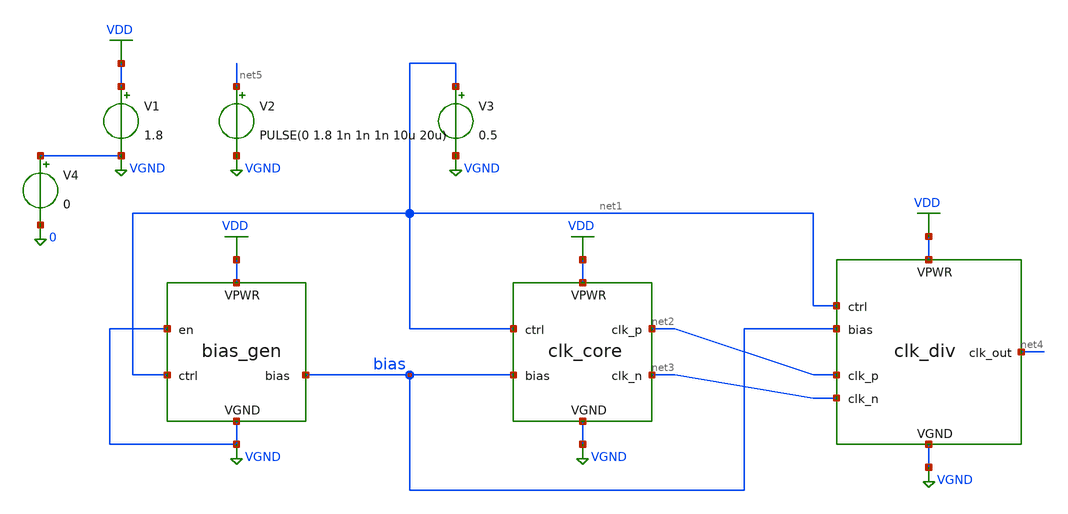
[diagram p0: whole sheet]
** sch_path: simple_vco/v1/tb_proto.sch
**.subckt tb_proto
x1 VDD VGND VGND net1 bias bias_gen
x2 VDD VGND net1 bias net2 net3 clk_core
x3 VDD VGND net1 bias net2 net3 net4 clk_div
V1 VDD VGND 1.8
V2 net5 VGND PULSE(0 1.8 1n 1n 1n 10u 20u)
V3 net1 VGND 0.5
V4 VGND 0 0
**** begin user architecture code


** opencircuitdesign pdks install

.lib $::SKYWATER_MODELS/sky130.lib.spice tt

.include $::SKYWATER_STDCELLS/sky130_fd_sc_hd.spice





.param mc_mm_switch=0

.control

save all

tran 50p 5u

plot CLK_OUT CLK_P CLK_N
plot bias

*quit 0

.endc

.end



**** end user architecture code
**.ends

* expanding   symbol:  bias_gen.sym # of pins=5
** sym_path: simple_vco/v1/bias_gen.sym
** sch_path: simple_vco/v1/bias_gen.sch
.subckt bias_gen VPWR VGND en ctrl bias_out
*.iopin VPWR
*.iopin VGND
*.ipin en
*.ipin ctrl
*.opin bias_out
XM8 net5 net5 VPWR VPWR sky130_fd_pr__pfet_01v8 L=0.15 W=1 nf=1 ad='int((1 + 1)/2) * 1 / 1 * 0.29' as='int((1 + 2)/2) * 1 / 1 * 0.29'
+ pd='2*int((1 + 1)/2) * (1 / 1 + 0.29)' ps='2*int((1 + 2)/2) * (1 / 1 + 0.29)' nrd='0.29 / 1 ' nrs='0.29 / 1 '
+ sa=0 sb=0 sd=0 mult=1 m=1
XM7 bias_out ctrl net3 VPWR sky130_fd_pr__pfet_01v8 L=0.15 W=1 nf=1 ad='int((1 + 1)/2) * 1 / 1 * 0.29'
+ as='int((1 + 2)/2) * 1 / 1 * 0.29' pd='2*int((1 + 1)/2) * (1 / 1 + 0.29)' ps='2*int((1 + 2)/2) * (1 / 1 + 0.29)'
+ nrd='0.29 / 1 ' nrs='0.29 / 1 ' sa=0 sb=0 sd=0 mult=1 m=1
XM6 net4 net1 net3 VPWR sky130_fd_pr__pfet_01v8 L=0.15 W=1 nf=1 ad='int((1 + 1)/2) * 1 / 1 * 0.29' as='int((1 + 2)/2) * 1 / 1 * 0.29'
+ pd='2*int((1 + 1)/2) * (1 / 1 + 0.29)' ps='2*int((1 + 2)/2) * (1 / 1 + 0.29)' nrd='0.29 / 1 ' nrs='0.29 / 1 '
+ sa=0 sb=0 sd=0 mult=1 m=1
XM3 net1 ctrl VPWR VPWR sky130_fd_pr__pfet_01v8 L=0.15 W=1 nf=1 ad='int((1 + 1)/2) * 1 / 1 * 0.29' as='int((1 + 2)/2) * 1 / 1 * 0.29'
+ pd='2*int((1 + 1)/2) * (1 / 1 + 0.29)' ps='2*int((1 + 2)/2) * (1 / 1 + 0.29)' nrd='0.29 / 1 ' nrs='0.29 / 1 '
+ sa=0 sb=0 sd=0 mult=1 m=1
XM1 net1 net1 VPWR VPWR sky130_fd_pr__pfet_01v8 L=0.15 W=1 nf=1 ad='int((1 + 1)/2) * 1 / 1 * 0.29' as='int((1 + 2)/2) * 1 / 1 * 0.29'
+ pd='2*int((1 + 1)/2) * (1 / 1 + 0.29)' ps='2*int((1 + 2)/2) * (1 / 1 + 0.29)' nrd='0.29 / 1 ' nrs='0.29 / 1 '
+ sa=0 sb=0 sd=0 mult=1 m=1
XM5 net3 net5 VPWR VPWR sky130_fd_pr__pfet_01v8 L=0.15 W=1 nf=1 ad='int((1 + 1)/2) * 1 / 1 * 0.29' as='int((1 + 2)/2) * 1 / 1 * 0.29'
+ pd='2*int((1 + 1)/2) * (1 / 1 + 0.29)' ps='2*int((1 + 2)/2) * (1 / 1 + 0.29)' nrd='0.29 / 1 ' nrs='0.29 / 1 '
+ sa=0 sb=0 sd=0 mult=1 m=1
XM9 bias_out net4 VGND VGND sky130_fd_pr__nfet_01v8 L=0.15 W=1 nf=1 ad='int((1 + 1)/2) * 1 / 1 * 0.29'
+ as='int((1 + 2)/2) * 1 / 1 * 0.29' pd='2*int((1 + 1)/2) * (1 / 1 + 0.29)' ps='2*int((1 + 2)/2) * (1 / 1 + 0.29)'
+ nrd='0.29 / 1 ' nrs='0.29 / 1 ' sa=0 sb=0 sd=0 mult=1 m=1
XM10 net4 net4 VGND VGND sky130_fd_pr__nfet_01v8 L=0.15 W=1 nf=1 ad='int((1 + 1)/2) * 1 / 1 * 0.29' as='int((1 + 2)/2) * 1 / 1 * 0.29'
+ pd='2*int((1 + 1)/2) * (1 / 1 + 0.29)' ps='2*int((1 + 2)/2) * (1 / 1 + 0.29)' nrd='0.29 / 1 ' nrs='0.29 / 1 '
+ sa=0 sb=0 sd=0 mult=1 m=1
XM11 net5 VPWR net6 VGND sky130_fd_pr__nfet_01v8 L=0.15 W=1 nf=1 ad='int((1 + 1)/2) * 1 / 1 * 0.29' as='int((1 + 2)/2) * 1 / 1 * 0.29'
+ pd='2*int((1 + 1)/2) * (1 / 1 + 0.29)' ps='2*int((1 + 2)/2) * (1 / 1 + 0.29)' nrd='0.29 / 1 ' nrs='0.29 / 1 '
+ sa=0 sb=0 sd=0 mult=1 m=1
XM12 net6 bias_out VGND VGND sky130_fd_pr__nfet_01v8 L=0.15 W=1 nf=1 ad='int((1 + 1)/2) * 1 / 1 * 0.29'
+ as='int((1 + 2)/2) * 1 / 1 * 0.29' pd='2*int((1 + 1)/2) * (1 / 1 + 0.29)' ps='2*int((1 + 2)/2) * (1 / 1 + 0.29)'
+ nrd='0.29 / 1 ' nrs='0.29 / 1 ' sa=0 sb=0 sd=0 mult=1 m=1
XM13 net6 net7 VGND VGND sky130_fd_pr__nfet_01v8 L=0.15 W=1 nf=1 ad='int((1 + 1)/2) * 1 / 1 * 0.29' as='int((1 + 2)/2) * 1 / 1 * 0.29'
+ pd='2*int((1 + 1)/2) * (1 / 1 + 0.29)' ps='2*int((1 + 2)/2) * (1 / 1 + 0.29)' nrd='0.29 / 1 ' nrs='0.29 / 1 '
+ sa=0 sb=0 sd=0 mult=1 m=1
XM14 net7 net8 VPWR VPWR sky130_fd_pr__pfet_01v8 L=0.15 W=1 nf=1 ad='int((1 + 1)/2) * 1 / 1 * 0.29' as='int((1 + 2)/2) * 1 / 1 * 0.29'
+ pd='2*int((1 + 1)/2) * (1 / 1 + 0.29)' ps='2*int((1 + 2)/2) * (1 / 1 + 0.29)' nrd='0.29 / 1 ' nrs='0.29 / 1 '
+ sa=0 sb=0 sd=0 mult=1 m=1
XM15 net7 net8 VGND VGND sky130_fd_pr__nfet_01v8 L=0.15 W=1 nf=1 ad='int((1 + 1)/2) * 1 / 1 * 0.29' as='int((1 + 2)/2) * 1 / 1 * 0.29'
+ pd='2*int((1 + 1)/2) * (1 / 1 + 0.29)' ps='2*int((1 + 2)/2) * (1 / 1 + 0.29)' nrd='0.29 / 1 ' nrs='0.29 / 1 '
+ sa=0 sb=0 sd=0 mult=1 m=1
XM16 net8 net9 VPWR VPWR sky130_fd_pr__pfet_01v8 L=0.15 W=1 nf=1 ad='int((1 + 1)/2) * 1 / 1 * 0.29' as='int((1 + 2)/2) * 1 / 1 * 0.29'
+ pd='2*int((1 + 1)/2) * (1 / 1 + 0.29)' ps='2*int((1 + 2)/2) * (1 / 1 + 0.29)' nrd='0.29 / 1 ' nrs='0.29 / 1 '
+ sa=0 sb=0 sd=0 mult=1 m=1
XM17 net8 net9 VGND VGND sky130_fd_pr__nfet_01v8 L=0.15 W=1 nf=1 ad='int((1 + 1)/2) * 1 / 1 * 0.29' as='int((1 + 2)/2) * 1 / 1 * 0.29'
+ pd='2*int((1 + 1)/2) * (1 / 1 + 0.29)' ps='2*int((1 + 2)/2) * (1 / 1 + 0.29)' nrd='0.29 / 1 ' nrs='0.29 / 1 '
+ sa=0 sb=0 sd=0 mult=1 m=1
XM19 net9 bias_out VGND VGND sky130_fd_pr__nfet_01v8 L=0.15 W=1 nf=1 ad='int((1 + 1)/2) * 1 / 1 * 0.29'
+ as='int((1 + 2)/2) * 1 / 1 * 0.29' pd='2*int((1 + 1)/2) * (1 / 1 + 0.29)' ps='2*int((1 + 2)/2) * (1 / 1 + 0.29)'
+ nrd='0.29 / 1 ' nrs='0.29 / 1 ' sa=0 sb=0 sd=0 mult=1 m=1
XM18 net9 en VPWR VPWR sky130_fd_pr__pfet_01v8_hvt L=8 W=0.42 nf=1 ad='int((1 + 1)/2) * 0.42 / 1 * 0.29'
+ as='int((1 + 2)/2) * 0.42 / 1 * 0.29' pd='2*int((1 + 1)/2) * (0.42 / 1 + 0.29)' ps='2*int((1 + 2)/2) * (0.42 / 1 + 0.29)'
+ nrd='0.29 / 0.42 ' nrs='0.29 / 0.42 ' sa=0 sb=0 sd=0 mult=1 m=1
XM20 bias_out en VGND VGND sky130_fd_pr__nfet_01v8 L=0.15 W=0.42 nf=1 ad='int((1 + 1)/2) * 0.42 / 1 * 0.29'
+ as='int((1 + 2)/2) * 0.42 / 1 * 0.29' pd='2*int((1 + 1)/2) * (0.42 / 1 + 0.29)' ps='2*int((1 + 2)/2) * (0.42 / 1 + 0.29)'
+ nrd='0.29 / 0.42 ' nrs='0.29 / 0.42 ' sa=0 sb=0 sd=0 mult=1 m=1
XM21 net9 en VGND VGND sky130_fd_pr__nfet_01v8 L=0.15 W=0.42 nf=1 ad='int((1 + 1)/2) * 0.42 / 1 * 0.29'
+ as='int((1 + 2)/2) * 0.42 / 1 * 0.29' pd='2*int((1 + 1)/2) * (0.42 / 1 + 0.29)' ps='2*int((1 + 2)/2) * (0.42 / 1 + 0.29)'
+ nrd='0.29 / 0.42 ' nrs='0.29 / 0.42 ' sa=0 sb=0 sd=0 mult=1 m=1
XM4 net2 bias_out VGND VGND sky130_fd_pr__nfet_01v8 L=0.15 W=1 nf=1 ad='int((1 + 1)/2) * 1 / 1 * 0.29'
+ as='int((1 + 2)/2) * 1 / 1 * 0.29' pd='2*int((1 + 1)/2) * (1 / 1 + 0.29)' ps='2*int((1 + 2)/2) * (1 / 1 + 0.29)'
+ nrd='0.29 / 1 ' nrs='0.29 / 1 ' sa=0 sb=0 sd=0 mult=1 m=1
XM2 net1 VPWR net2 VGND sky130_fd_pr__nfet_01v8 L=0.15 W=1 nf=1 ad='int((1 + 1)/2) * 1 / 1 * 0.29' as='int((1 + 2)/2) * 1 / 1 * 0.29'
+ pd='2*int((1 + 1)/2) * (1 / 1 + 0.29)' ps='2*int((1 + 2)/2) * (1 / 1 + 0.29)' nrd='0.29 / 1 ' nrs='0.29 / 1 '
+ sa=0 sb=0 sd=0 mult=1 m=1
.ends


* expanding   symbol:  clk_core.sym # of pins=6
** sym_path: simple_vco/v1/clk_core.sym
** sch_path: simple_vco/v1/clk_core.sch
.subckt clk_core VPWR VGND ctrl bias_in clk_p clk_n
*.iopin VPWR
*.iopin VGND
*.ipin ctrl
*.ipin bias_in
*.opin clk_p
*.opin clk_n
XM3 clk_n ctrl VPWR VPWR sky130_fd_pr__pfet_01v8 L=0.15 W=1 nf=1 ad='int((1 + 1)/2) * 1 / 1 * 0.29' as='int((1 + 2)/2) * 1 / 1 * 0.29'
+ pd='2*int((1 + 1)/2) * (1 / 1 + 0.29)' ps='2*int((1 + 2)/2) * (1 / 1 + 0.29)' nrd='0.29 / 1 ' nrs='0.29 / 1 '
+ sa=0 sb=0 sd=0 mult=1 m=1
XM1 clk_n clk_n VPWR VPWR sky130_fd_pr__pfet_01v8 L=0.15 W=1 nf=1 ad='int((1 + 1)/2) * 1 / 1 * 0.29'
+ as='int((1 + 2)/2) * 1 / 1 * 0.29' pd='2*int((1 + 1)/2) * (1 / 1 + 0.29)' ps='2*int((1 + 2)/2) * (1 / 1 + 0.29)'
+ nrd='0.29 / 1 ' nrs='0.29 / 1 ' sa=0 sb=0 sd=0 mult=1 m=1
XM4 net3 bias_in VGND VGND sky130_fd_pr__nfet_01v8 L=0.15 W=1 nf=1 ad='int((1 + 1)/2) * 1 / 1 * 0.29'
+ as='int((1 + 2)/2) * 1 / 1 * 0.29' pd='2*int((1 + 1)/2) * (1 / 1 + 0.29)' ps='2*int((1 + 2)/2) * (1 / 1 + 0.29)'
+ nrd='0.29 / 1 ' nrs='0.29 / 1 ' sa=0 sb=0 sd=0 mult=1 m=1
XM2 clk_n net1 net3 VGND sky130_fd_pr__nfet_01v8 L=0.15 W=1 nf=1 ad='int((1 + 1)/2) * 1 / 1 * 0.29' as='int((1 + 2)/2) * 1 / 1 * 0.29'
+ pd='2*int((1 + 1)/2) * (1 / 1 + 0.29)' ps='2*int((1 + 2)/2) * (1 / 1 + 0.29)' nrd='0.29 / 1 ' nrs='0.29 / 1 '
+ sa=0 sb=0 sd=0 mult=1 m=1
XM5 VPWR ctrl VPWR VPWR sky130_fd_pr__pfet_01v8 L=0.15 W=1 nf=1 ad='int((1 + 1)/2) * 1 / 1 * 0.29' as='int((1 + 2)/2) * 1 / 1 * 0.29'
+ pd='2*int((1 + 1)/2) * (1 / 1 + 0.29)' ps='2*int((1 + 2)/2) * (1 / 1 + 0.29)' nrd='0.29 / 1 ' nrs='0.29 / 1 '
+ sa=0 sb=0 sd=0 mult=1 m=1
XM6 VPWR VPWR VPWR VPWR sky130_fd_pr__pfet_01v8 L=0.15 W=1 nf=1 ad='int((1 + 1)/2) * 1 / 1 * 0.29' as='int((1 + 2)/2) * 1 / 1 * 0.29'
+ pd='2*int((1 + 1)/2) * (1 / 1 + 0.29)' ps='2*int((1 + 2)/2) * (1 / 1 + 0.29)' nrd='0.29 / 1 ' nrs='0.29 / 1 '
+ sa=0 sb=0 sd=0 mult=1 m=1
XM8 VPWR net2 net3 VGND sky130_fd_pr__nfet_01v8 L=0.15 W=1 nf=1 ad='int((1 + 1)/2) * 1 / 1 * 0.29' as='int((1 + 2)/2) * 1 / 1 * 0.29'
+ pd='2*int((1 + 1)/2) * (1 / 1 + 0.29)' ps='2*int((1 + 2)/2) * (1 / 1 + 0.29)' nrd='0.29 / 1 ' nrs='0.29 / 1 '
+ sa=0 sb=0 sd=0 mult=1 m=1
XM7 VPWR clk_n net3 VGND sky130_fd_pr__nfet_01v8 L=0.15 W=1 nf=1 ad='int((1 + 1)/2) * 1 / 1 * 0.29' as='int((1 + 2)/2) * 1 / 1 * 0.29'
+ pd='2*int((1 + 1)/2) * (1 / 1 + 0.29)' ps='2*int((1 + 2)/2) * (1 / 1 + 0.29)' nrd='0.29 / 1 ' nrs='0.29 / 1 '
+ sa=0 sb=0 sd=0 mult=1 m=1
XM9 clk_n VPWR net3 VGND sky130_fd_pr__nfet_01v8 L=0.15 W=1 nf=1 ad='int((1 + 1)/2) * 1 / 1 * 0.29' as='int((1 + 2)/2) * 1 / 1 * 0.29'
+ pd='2*int((1 + 1)/2) * (1 / 1 + 0.29)' ps='2*int((1 + 2)/2) * (1 / 1 + 0.29)' nrd='0.29 / 1 ' nrs='0.29 / 1 '
+ sa=0 sb=0 sd=0 mult=1 m=1
XM10 net1 ctrl VPWR VPWR sky130_fd_pr__pfet_01v8 L=0.15 W=1 nf=1 ad='int((1 + 1)/2) * 1 / 1 * 0.29' as='int((1 + 2)/2) * 1 / 1 * 0.29'
+ pd='2*int((1 + 1)/2) * (1 / 1 + 0.29)' ps='2*int((1 + 2)/2) * (1 / 1 + 0.29)' nrd='0.29 / 1 ' nrs='0.29 / 1 '
+ sa=0 sb=0 sd=0 mult=1 m=1
XM11 net1 net1 VPWR VPWR sky130_fd_pr__pfet_01v8 L=0.15 W=1 nf=1 ad='int((1 + 1)/2) * 1 / 1 * 0.29' as='int((1 + 2)/2) * 1 / 1 * 0.29'
+ pd='2*int((1 + 1)/2) * (1 / 1 + 0.29)' ps='2*int((1 + 2)/2) * (1 / 1 + 0.29)' nrd='0.29 / 1 ' nrs='0.29 / 1 '
+ sa=0 sb=0 sd=0 mult=1 m=1
XM12 net4 bias_in VGND VGND sky130_fd_pr__nfet_01v8 L=0.15 W=1 nf=1 ad='int((1 + 1)/2) * 1 / 1 * 0.29'
+ as='int((1 + 2)/2) * 1 / 1 * 0.29' pd='2*int((1 + 1)/2) * (1 / 1 + 0.29)' ps='2*int((1 + 2)/2) * (1 / 1 + 0.29)'
+ nrd='0.29 / 1 ' nrs='0.29 / 1 ' sa=0 sb=0 sd=0 mult=1 m=1
XM13 net1 VPWR net4 VGND sky130_fd_pr__nfet_01v8 L=0.15 W=1 nf=1 ad='int((1 + 1)/2) * 1 / 1 * 0.29' as='int((1 + 2)/2) * 1 / 1 * 0.29'
+ pd='2*int((1 + 1)/2) * (1 / 1 + 0.29)' ps='2*int((1 + 2)/2) * (1 / 1 + 0.29)' nrd='0.29 / 1 ' nrs='0.29 / 1 '
+ sa=0 sb=0 sd=0 mult=1 m=1
XM14 net2 ctrl VPWR VPWR sky130_fd_pr__pfet_01v8 L=0.15 W=1 nf=1 ad='int((1 + 1)/2) * 1 / 1 * 0.29' as='int((1 + 2)/2) * 1 / 1 * 0.29'
+ pd='2*int((1 + 1)/2) * (1 / 1 + 0.29)' ps='2*int((1 + 2)/2) * (1 / 1 + 0.29)' nrd='0.29 / 1 ' nrs='0.29 / 1 '
+ sa=0 sb=0 sd=0 mult=1 m=1
XM15 net2 net2 VPWR VPWR sky130_fd_pr__pfet_01v8 L=0.15 W=1 nf=1 ad='int((1 + 1)/2) * 1 / 1 * 0.29' as='int((1 + 2)/2) * 1 / 1 * 0.29'
+ pd='2*int((1 + 1)/2) * (1 / 1 + 0.29)' ps='2*int((1 + 2)/2) * (1 / 1 + 0.29)' nrd='0.29 / 1 ' nrs='0.29 / 1 '
+ sa=0 sb=0 sd=0 mult=1 m=1
XM16 net2 clk_n net4 VGND sky130_fd_pr__nfet_01v8 L=0.15 W=1 nf=1 ad='int((1 + 1)/2) * 1 / 1 * 0.29'
+ as='int((1 + 2)/2) * 1 / 1 * 0.29' pd='2*int((1 + 1)/2) * (1 / 1 + 0.29)' ps='2*int((1 + 2)/2) * (1 / 1 + 0.29)'
+ nrd='0.29 / 1 ' nrs='0.29 / 1 ' sa=0 sb=0 sd=0 mult=1 m=1
XM17 net2 net1 net4 VGND sky130_fd_pr__nfet_01v8 L=0.15 W=1 nf=1 ad='int((1 + 1)/2) * 1 / 1 * 0.29' as='int((1 + 2)/2) * 1 / 1 * 0.29'
+ pd='2*int((1 + 1)/2) * (1 / 1 + 0.29)' ps='2*int((1 + 2)/2) * (1 / 1 + 0.29)' nrd='0.29 / 1 ' nrs='0.29 / 1 '
+ sa=0 sb=0 sd=0 mult=1 m=1
XM18 net1 net2 net4 VGND sky130_fd_pr__nfet_01v8 L=0.15 W=1 nf=1 ad='int((1 + 1)/2) * 1 / 1 * 0.29' as='int((1 + 2)/2) * 1 / 1 * 0.29'
+ pd='2*int((1 + 1)/2) * (1 / 1 + 0.29)' ps='2*int((1 + 2)/2) * (1 / 1 + 0.29)' nrd='0.29 / 1 ' nrs='0.29 / 1 '
+ sa=0 sb=0 sd=0 mult=1 m=1
.ends


* expanding   symbol:  clk_div.sym # of pins=7
** sym_path: simple_vco/v1/clk_div.sym
** sch_path: simple_vco/v1/clk_div.sch
.subckt clk_div VPWR VGND ctrl bias_in clk_p clk_n clk_out
*.iopin VPWR
*.iopin VGND
*.ipin ctrl
*.ipin bias_in
*.ipin clk_p
*.ipin clk_n
*.opin clk_out
.ends

.GLOBAL VGND
.GLOBAL VDD
.end
